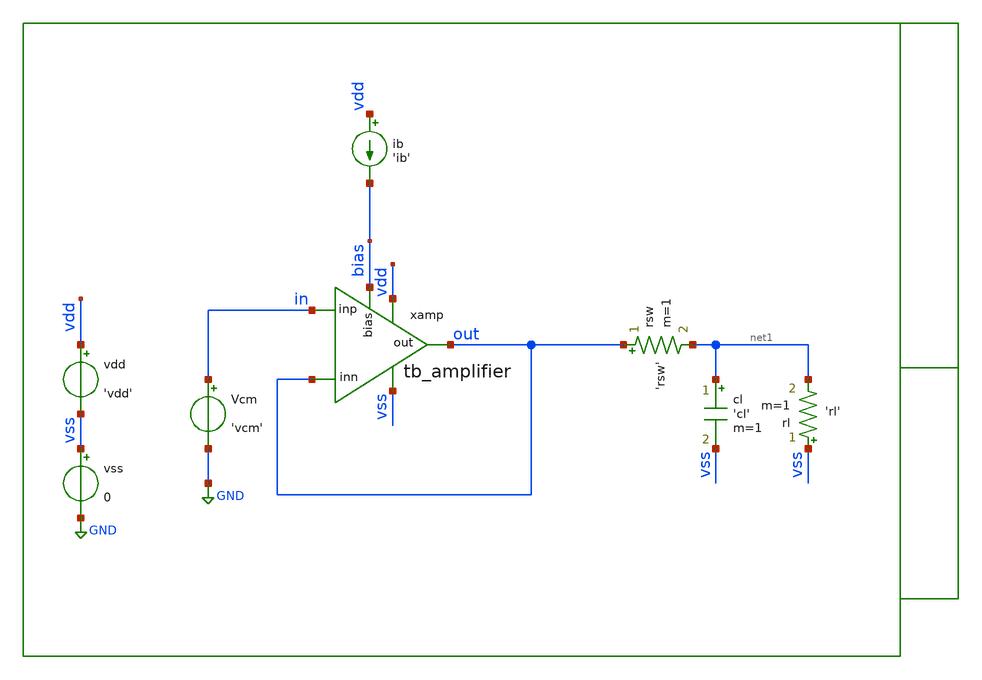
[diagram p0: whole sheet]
** sch_path: xschem/tb/testbuffer/tb_amplifier/op_tb_amplifier_power.sch
**.subckt op_tb_amplifier_power
ib vdd bias 'ib'
xamp vdd out in out vss bias tb_amplifier
Vcm in GND 'vcm'
vdd vdd vss 'vdd'
vss vss GND 0
cl net1 vss 'cl' m=1
rl vss net1 'rl' m=1
rsw out net1 'rsw' m=1
**** begin user architecture code

* Control

.param vdd=3.3
.param vcm='vdd/2'
.param ib=5u
.param cl=10p
.param rl=1e6
.param rsw=1

.control
save all
op

let vsup = v(vdd)

let id_xm4 = @m.xamp.xm4.m0[id]
let id_xmb1 = @m.xamp.xmb1.m0[id]
let id_xm5 = @m.xamp.xm5.m0[id]
let id_xm6 = @m.xamp.xm6.m0[id]
let id_xm1 = @m.xamp.xm1.m0[id]
let id_xm2 = @m.xamp.xm2.m0[id]
let id_xm3 = @m.xamp.xm3.m0[id]
let id_xm7 = @m.xamp.xm7.m0[id]
let id_xmb2 = @m.xamp.xmb2.m0[id]
let id_xmb3 = @m.xamp.xmb3.m0[id]
let id_xmb4 = @m.xamp.xmb4.m0[id]

print id_xm1
print id_xm2
print id_xm4
print id_xmb1
print id_xm5
print id_xm6
print id_xm1
print id_xm2
print id_xm3
print id_xm7
print id_xmb2
print id_xmb3
print id_xmb4

let itot = id_xmb1 + id_xmb4 + id_xm3 + id_xm4 + id_xm7
let ptot = itot*vsup

print itot
print ptot

.endc


 * Model Corners

.include $::CORNERS/ngspice/tt.spice
*.include $::CORNERS/ngspice/ff.spice
*.include $::CORNERS/ngspice/ss.spice
*.include $::CORNERS/ngspice/sf.spice
*.include $::CORNERS/ngspice/fs.spice

**** end user architecture code
**.ends

* expanding   symbol:  sch/testbuffer/tb_amplifier/tb_amplifier.sym # of pins=6
** sym_path: xschem/sch/testbuffer/tb_amplifier/tb_amplifier.sym
** sch_path: xschem/sch/testbuffer/tb_amplifier/tb_amplifier.sch
.subckt tb_amplifier vdd out inp inn vss bias
*.ipin inn
*.ipin inp
*.opin out
*.iopin bias
*.iopin vdd
*.iopin vss
XM3 mirr mirr vdd vdd pfet_06v0 L=4u W=16u nf=2 ad='int((nf+1)/2) * W/nf * 0.18u' as='int((nf+2)/2) * W/nf * 0.18u'
+ pd='2*int((nf+1)/2) * (W/nf + 0.18u)' ps='2*int((nf+2)/2) * (W/nf + 0.18u)' nrd='0.18u / W' nrs='0.18u / W'
+ sa=0 sb=0 sd=0 m=2 par=2
XM4 comp mirr vdd vdd pfet_06v0 L=4u W=16u nf=2 ad='int((nf+1)/2) * W/nf * 0.18u' as='int((nf+2)/2) * W/nf * 0.18u'
+ pd='2*int((nf+1)/2) * (W/nf + 0.18u)' ps='2*int((nf+2)/2) * (W/nf + 0.18u)' nrd='0.18u / W' nrs='0.18u / W'
+ sa=0 sb=0 sd=0 m=2 par=2
XM2 comp inp vcm vss nfet_06v0 L=2u W=16u nf=2 ad='int((nf+1)/2) * W/nf * 0.18u' as='int((nf+2)/2) * W/nf * 0.18u'
+ pd='2*int((nf+1)/2) * (W/nf + 0.18u)' ps='2*int((nf+2)/2) * (W/nf + 0.18u)' nrd='0.18u / W' nrs='0.18u / W'
+ sa=0 sb=0 sd=0 m=2 par=2
XM1 mirr inn vcm vss nfet_06v0 L=2u W=16u nf=2 ad='int((nf+1)/2) * W/nf * 0.18u' as='int((nf+2)/2) * W/nf * 0.18u'
+ pd='2*int((nf+1)/2) * (W/nf + 0.18u)' ps='2*int((nf+2)/2) * (W/nf + 0.18u)' nrd='0.18u / W' nrs='0.18u / W'
+ sa=0 sb=0 sd=0 m=2 par=2
XM5 vcm bias vss vss nfet_06v0 L=1u W=16u nf=2 ad='int((nf+1)/2) * W/nf * 0.18u' as='int((nf+2)/2) * W/nf * 0.18u'
+ pd='2*int((nf+1)/2) * (W/nf + 0.18u)' ps='2*int((nf+2)/2) * (W/nf + 0.18u)' nrd='0.18u / W' nrs='0.18u / W'
+ sa=0 sb=0 sd=0 m=2 par=2
XM6 out bias vss vss nfet_06v0 L=1u W=16u nf=2 ad='int((nf+1)/2) * W/nf * 0.18u' as='int((nf+2)/2) * W/nf * 0.18u'
+ pd='2*int((nf+1)/2) * (W/nf + 0.18u)' ps='2*int((nf+2)/2) * (W/nf + 0.18u)' nrd='0.18u / W' nrs='0.18u / W'
+ sa=0 sb=0 sd=0 m=12 par=12
XM7 out comp vdd vdd pfet_06v0 L=1u W=96u nf=12 ad='int((nf+1)/2) * W/nf * 0.18u' as='int((nf+2)/2) * W/nf * 0.18u'
+ pd='2*int((nf+1)/2) * (W/nf + 0.18u)' ps='2*int((nf+2)/2) * (W/nf + 0.18u)' nrd='0.18u / W' nrs='0.18u / W'
+ sa=0 sb=0 sd=0 m=1 par=1
XMB1 bias bias vss vss nfet_06v0 L=1u W=16u nf=2 ad='int((nf+1)/2) * W/nf * 0.18u' as='int((nf+2)/2) * W/nf * 0.18u'
+ pd='2*int((nf+1)/2) * (W/nf + 0.18u)' ps='2*int((nf+2)/2) * (W/nf + 0.18u)' nrd='0.18u / W' nrs='0.18u / W'
+ sa=0 sb=0 sd=0 m=2 par=2
XMB2 vbm bias vss vss nfet_06v0 L=1u W=16u nf=2 ad='int((nf+1)/2) * W/nf * 0.18u' as='int((nf+2)/2) * W/nf * 0.18u'
+ pd='2*int((nf+1)/2) * (W/nf + 0.18u)' ps='2*int((nf+2)/2) * (W/nf + 0.18u)' nrd='0.18u / W' nrs='0.18u / W'
+ sa=0 sb=0 sd=0 m=2 par=2
XMB3 vbm vbm vbt vdd pfet_06v0 L=1u W=16u nf=2 ad='int((nf+1)/2) * W/nf * 0.18u' as='int((nf+2)/2) * W/nf * 0.18u'
+ pd='2*int((nf+1)/2) * (W/nf + 0.18u)' ps='2*int((nf+2)/2) * (W/nf + 0.18u)' nrd='0.18u / W' nrs='0.18u / W'
+ sa=0 sb=0 sd=0 m=1 par=1
XMB4 vbt vbt vdd vdd pfet_06v0 L=1u W=16u nf=2 ad='int((nf+1)/2) * W/nf * 0.18u' as='int((nf+2)/2) * W/nf * 0.18u'
+ pd='2*int((nf+1)/2) * (W/nf + 0.18u)' ps='2*int((nf+2)/2) * (W/nf + 0.18u)' nrd='0.18u / W' nrs='0.18u / W'
+ sa=0 sb=0 sd=0 m=1 par=1
XRCC gc comp vdd ppolyf_u_1k_6p0 r_width=2e-6 r_length=38e-6 s=1 m=1
XMDUM1 vss vss vss vss nfet_06v0 L=2u W=16u nf=2 ad='int((nf+1)/2) * W/nf * 0.18u' as='int((nf+2)/2) * W/nf * 0.18u'
+ pd='2*int((nf+1)/2) * (W/nf + 0.18u)' ps='2*int((nf+2)/2) * (W/nf + 0.18u)' nrd='0.18u / W' nrs='0.18u / W'
+ sa=0 sb=0 sd=0 m=2 par=2
XMDUM2 vdd vdd vdd vdd pfet_06v0 L=4u W=16u nf=2 ad='int((nf+1)/2) * W/nf * 0.18u' as='int((nf+2)/2) * W/nf * 0.18u'
+ pd='2*int((nf+1)/2) * (W/nf + 0.18u)' ps='2*int((nf+2)/2) * (W/nf + 0.18u)' nrd='0.18u / W' nrs='0.18u / W'
+ sa=0 sb=0 sd=0 m=4 par=4
XC1 out gc cap_mim_2f0_m4m5_noshield c_width=30e-6 c_length=30e-6 m=1
.ends

.GLOBAL GND
.end
